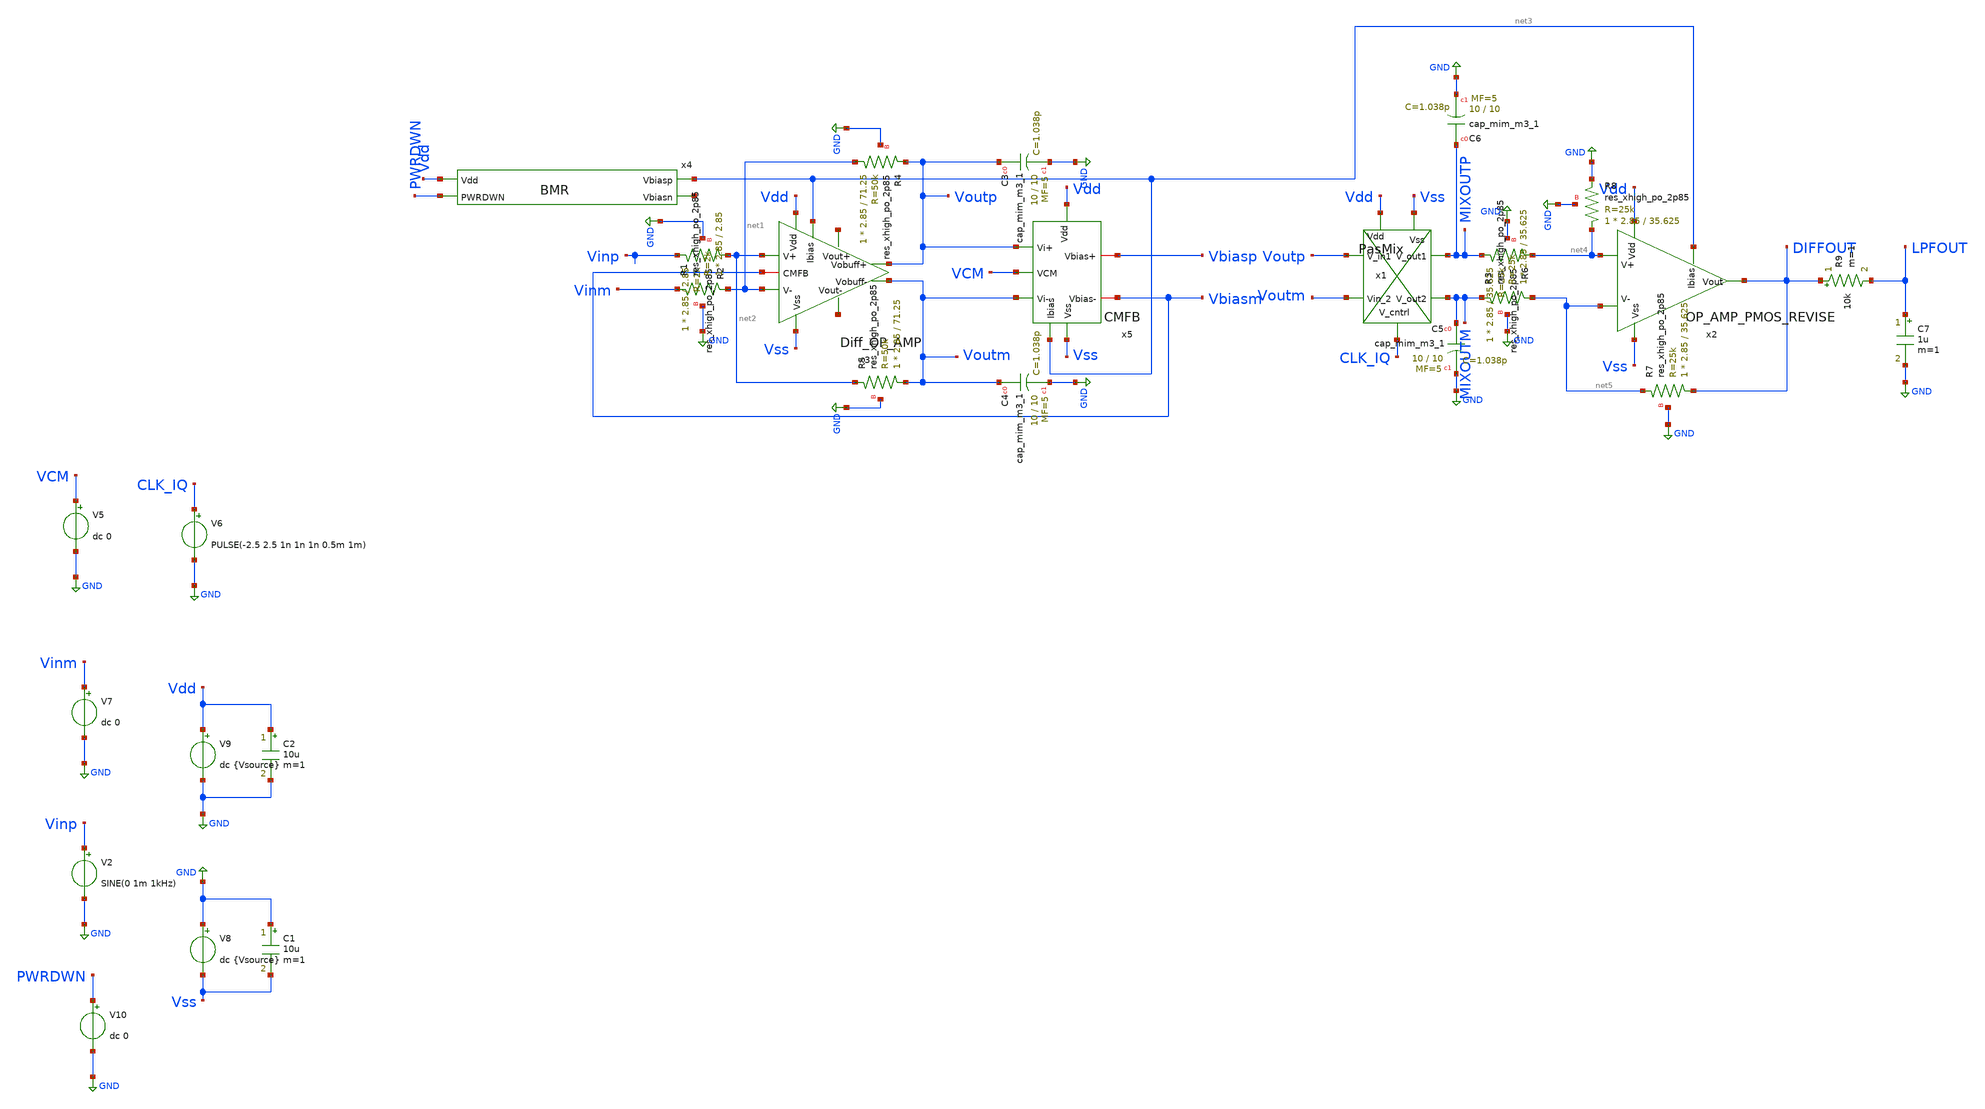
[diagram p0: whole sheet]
** sch_path: xschem/DiffTB.sch
**.subckt DiffTB
V5 VCM GND dc 0
V6 CLK_IQ GND PULSE(-2.5 2.5 1n 1n 1n 0.5m 1m)
V2 Vinp GND SINE(0 1m 1kHz)
V7 Vinm GND dc 0
V8 GND Vss dc {Vsource}
V9 Vdd GND dc {Vsource}
V10 PWRDWN GND dc 0
C1 GND Vss 10u m=1
C2 Vdd GND 10u m=1
x3 Vss Vbiasm net6 net7 net1 net2 Voutp Voutm net3 Vdd Diff_OP_AMP
x4 Vdd net3 net8 PWRDWN BMR
x5 Vss Vbiasp Vbiasm Voutm Voutp VCM net3 Vdd CMFB
XC3 Voutp GND sky130_fd_pr__cap_mim_m3_1 W=10 L=10 MF=5 m=5
XC4 Voutm GND sky130_fd_pr__cap_mim_m3_1 W=10 L=10 MF=5 m=5
XR4 net1 Voutp GND sky130_fd_pr__res_xhigh_po_2p85 L=71.25 mult=1 m=1
XR2 Vinp net2 GND sky130_fd_pr__res_xhigh_po_2p85 L=2.85 mult=1 m=1
XR5 Voutm net2 GND sky130_fd_pr__res_xhigh_po_2p85 L=71.25 mult=1 m=1
XR1 net1 Vinm GND sky130_fd_pr__res_xhigh_po_2p85 L=2.85 mult=1 m=1
x1 Vdd CLK_IQ Vss MIXOUTP Voutp MIXOUTM Voutm PasMix
x2 Vdd Vss net3 DIFFOUT net4 net5 OP_AMP_PMOS_REVISE
XR6 MIXOUTP net4 GND sky130_fd_pr__res_xhigh_po_2p85 L=35.625 mult=1 m=1
XR3 net5 MIXOUTM GND sky130_fd_pr__res_xhigh_po_2p85 L=35.625 mult=1 m=1
XR7 DIFFOUT net5 GND sky130_fd_pr__res_xhigh_po_2p85 L=35.625 mult=1 m=1
XR8 net4 GND GND sky130_fd_pr__res_xhigh_po_2p85 L=35.625 mult=1 m=1
XC5 MIXOUTM GND sky130_fd_pr__cap_mim_m3_1 W=10 L=10 MF=5 m=5
XC6 MIXOUTP GND sky130_fd_pr__cap_mim_m3_1 W=10 L=10 MF=5 m=5
R9 DIFFOUT LPFOUT 10k m=1
C7 LPFOUT GND 1u m=1
**** begin user architecture code


.lib /foss/pdks/sky130A/libs.tech/combined/sky130.lib.spice tt_mm

***Centered at 40C and varies to a range of -20 to 100; with 20C being 1-standard dev***
.param TEMPGAUSS = agauss(40, 60, 3)

***Centered at 2.5V and varies to a range of 2V to 3V; with 0.16mV being 1-standard dev***
.param VOLTGAUSS = agauss(2.5, 0.5, 3)

.param ptemp = 'TEMPGAUSS'

.param Vsource = 'VOLTGAUSS'
.options temp = {ptemp}

.csparam ctemp = {ptemp}
.csparam cvolt = {Vsource}


.control
 let T = 27
 let V = 2.5

 let i_count = 10

 let index = 0

 set wr_vecnames
 dowhile index <= 10
   save all
   tran 10u 50m
   *dc V1 0 6 0.01
   *ac dec 100 0.1 30MEG

   write POST_LPF_OFFSETS_TT_MM_PVT.raw

   set noprintscale

   set appendwrite


   let V = $&cvolt
   let T = $&ctemp

   echo -n This is $&V
   echo -n This is $&T
   echo -n This is $&index

   let index = index + 1
   reset
 end
  **OL AC
  *** print col GAIN_vec UGW_vec PM_vec T_vec V_vec > FDA_AC_CM_GAIN_UGW_PM_SS_PVT.txt
  **Offset
   *** print col OFFSETDIF_vec OFFSETMIX_vec OFFSETOUT_vec T_vec V_vec >
+ PRE_LPF_OFFSETS_SS_MM_PVT.txt

.endc
.end

**** end user architecture code
**.ends

* expanding   symbol:  Diff_OP_AMP.sym # of pins=10
** sym_path: xschem/Diff_OP_AMP.sym
** sch_path: xschem/Diff_OP_AMP.sch
.subckt Diff_OP_AMP Vss CMFB Vout- Vout+ V- V+ Vobuff+ Vobuff- Ibias Vdd
*.opin Vout+
*.ipin Vdd
*.ipin Vss
*.ipin V+
*.ipin V-
*.opin Vout-
*.ipin Ibias
*.opin Vobuff-
*.opin Vobuff+
*.iopin CMFB
XM4 net1 Ibias Vdd Vdd sky130_fd_pr__pfet_g5v0d10v5 L=3 W=31 nf=8 ad='int((8 + 1)/2) * 31 / 8 * 0.29'
+ as='int((8 + 2)/2) * 31 / 8 * 0.29' pd='2*int((8 + 1)/2) * (31 / 8 + 0.29)' ps='2*int((8 + 2)/2) * (31 / 8 + 0.29)'
+ nrd='0.29 / 31 ' nrs='0.29 / 31 ' sa=0 sb=0 sd=0 mult=2 m=2
XM18 net2 V- net1 net1 sky130_fd_pr__pfet_g5v0d10v5 L=3 W=80 nf=8 ad='int((8 + 1)/2) * 80 / 8 * 0.29'
+ as='int((8 + 2)/2) * 80 / 8 * 0.29' pd='2*int((8 + 1)/2) * (80 / 8 + 0.29)' ps='2*int((8 + 2)/2) * (80 / 8 + 0.29)'
+ nrd='0.29 / 80 ' nrs='0.29 / 80 ' sa=0 sb=0 sd=0 mult=4 m=4
XM1 net3 V+ net1 net1 sky130_fd_pr__pfet_g5v0d10v5 L=3 W=80 nf=8 ad='int((8 + 1)/2) * 80 / 8 * 0.29'
+ as='int((8 + 2)/2) * 80 / 8 * 0.29' pd='2*int((8 + 1)/2) * (80 / 8 + 0.29)' ps='2*int((8 + 2)/2) * (80 / 8 + 0.29)'
+ nrd='0.29 / 80 ' nrs='0.29 / 80 ' sa=0 sb=0 sd=0 mult=4 m=4
XM11 net2 CMFB Vss Vss sky130_fd_pr__nfet_g5v0d10v5 L=6 W=0.81 nf=1 ad='int((1 + 1)/2) * 0.81 / 1 * 0.29'
+ as='int((1 + 2)/2) * 0.81 / 1 * 0.29' pd='2*int((1 + 1)/2) * (0.81 / 1 + 0.29)' ps='2*int((1 + 2)/2) * (0.81 / 1 + 0.29)'
+ nrd='0.29 / 0.81 ' nrs='0.29 / 0.81 ' sa=0 sb=0 sd=0 mult=2 m=2
XM3 net3 CMFB Vss Vss sky130_fd_pr__nfet_g5v0d10v5 L=6 W=0.81 nf=1 ad='int((1 + 1)/2) * 0.81 / 1 * 0.29'
+ as='int((1 + 2)/2) * 0.81 / 1 * 0.29' pd='2*int((1 + 1)/2) * (0.81 / 1 + 0.29)' ps='2*int((1 + 2)/2) * (0.81 / 1 + 0.29)'
+ nrd='0.29 / 0.81 ' nrs='0.29 / 0.81 ' sa=0 sb=0 sd=0 mult=2 m=2
XM13 Vout+ net2 Vss Vss sky130_fd_pr__nfet_g5v0d10v5 L=3 W=14 nf=2 ad='int((2 + 1)/2) * 14 / 2 * 0.29'
+ as='int((2 + 2)/2) * 14 / 2 * 0.29' pd='2*int((2 + 1)/2) * (14 / 2 + 0.29)' ps='2*int((2 + 2)/2) * (14 / 2 + 0.29)'
+ nrd='0.29 / 14 ' nrs='0.29 / 14 ' sa=0 sb=0 sd=0 mult=2 m=2
XM2 Vout- net3 Vss Vss sky130_fd_pr__nfet_g5v0d10v5 L=3 W=14 nf=2 ad='int((2 + 1)/2) * 14 / 2 * 0.29'
+ as='int((2 + 2)/2) * 14 / 2 * 0.29' pd='2*int((2 + 1)/2) * (14 / 2 + 0.29)' ps='2*int((2 + 2)/2) * (14 / 2 + 0.29)'
+ nrd='0.29 / 14 ' nrs='0.29 / 14 ' sa=0 sb=0 sd=0 mult=2 m=2
XM5 net5 Ibias Vdd Vdd sky130_fd_pr__pfet_g5v0d10v5 L=3 W=31 nf=8 ad='int((8 + 1)/2) * 31 / 8 * 0.29'
+ as='int((8 + 2)/2) * 31 / 8 * 0.29' pd='2*int((8 + 1)/2) * (31 / 8 + 0.29)' ps='2*int((8 + 2)/2) * (31 / 8 + 0.29)'
+ nrd='0.29 / 31 ' nrs='0.29 / 31 ' sa=0 sb=0 sd=0 mult=30 m=30
XM6 net7 Ibias Vdd Vdd sky130_fd_pr__pfet_g5v0d10v5 L=3 W=31 nf=8 ad='int((8 + 1)/2) * 31 / 8 * 0.29'
+ as='int((8 + 2)/2) * 31 / 8 * 0.29' pd='2*int((8 + 1)/2) * (31 / 8 + 0.29)' ps='2*int((8 + 2)/2) * (31 / 8 + 0.29)'
+ nrd='0.29 / 31 ' nrs='0.29 / 31 ' sa=0 sb=0 sd=0 mult=30 m=30
XM8 Vout+ Vout+ net4 net4 sky130_fd_pr__pfet_g5v0d10v5 L=3 W=41.1 nf=4 ad='int((4 + 1)/2) * 41.1 / 4 * 0.29'
+ as='int((4 + 2)/2) * 41.1 / 4 * 0.29' pd='2*int((4 + 1)/2) * (41.1 / 4 + 0.29)' ps='2*int((4 + 2)/2) * (41.1 / 4 + 0.29)'
+ nrd='0.29 / 41.1 ' nrs='0.29 / 41.1 ' sa=0 sb=0 sd=0 mult=4 m=4
XM7 Vss Vout+ Vobuff- Vobuff- sky130_fd_pr__pfet_g5v0d10v5 L=3 W=41.1 nf=4 ad='int((4 + 1)/2) * 41.1 / 4 * 0.29'
+ as='int((4 + 2)/2) * 41.1 / 4 * 0.29' pd='2*int((4 + 1)/2) * (41.1 / 4 + 0.29)' ps='2*int((4 + 2)/2) * (41.1 / 4 + 0.29)'
+ nrd='0.29 / 41.1 ' nrs='0.29 / 41.1 ' sa=0 sb=0 sd=0 mult=4 m=4
XM9 Vss Vout- Vobuff+ Vobuff+ sky130_fd_pr__pfet_g5v0d10v5 L=3 W=41.1 nf=4 ad='int((4 + 1)/2) * 41.1 / 4 * 0.29'
+ as='int((4 + 2)/2) * 41.1 / 4 * 0.29' pd='2*int((4 + 1)/2) * (41.1 / 4 + 0.29)' ps='2*int((4 + 2)/2) * (41.1 / 4 + 0.29)'
+ nrd='0.29 / 41.1 ' nrs='0.29 / 41.1 ' sa=0 sb=0 sd=0 mult=4 m=4
XM12 Vout- Vout- net6 net6 sky130_fd_pr__pfet_g5v0d10v5 L=3 W=41.1 nf=4 ad='int((4 + 1)/2) * 41.1 / 4 * 0.29'
+ as='int((4 + 2)/2) * 41.1 / 4 * 0.29' pd='2*int((4 + 1)/2) * (41.1 / 4 + 0.29)' ps='2*int((4 + 2)/2) * (41.1 / 4 + 0.29)'
+ nrd='0.29 / 41.1 ' nrs='0.29 / 41.1 ' sa=0 sb=0 sd=0 mult=4 m=4
XM16 net5 net5 net4 net4 sky130_fd_pr__nfet_g5v0d10v5 L=3 W=18 nf=4 ad='int((4 + 1)/2) * 18 / 4 * 0.29'
+ as='int((4 + 2)/2) * 18 / 4 * 0.29' pd='2*int((4 + 1)/2) * (18 / 4 + 0.29)' ps='2*int((4 + 2)/2) * (18 / 4 + 0.29)'
+ nrd='0.29 / 18 ' nrs='0.29 / 18 ' sa=0 sb=0 sd=0 mult=2 m=2
XM14 Vdd net5 Vobuff- Vobuff- sky130_fd_pr__nfet_g5v0d10v5 L=3 W=18 nf=4 ad='int((4 + 1)/2) * 18 / 4 * 0.29'
+ as='int((4 + 2)/2) * 18 / 4 * 0.29' pd='2*int((4 + 1)/2) * (18 / 4 + 0.29)' ps='2*int((4 + 2)/2) * (18 / 4 + 0.29)'
+ nrd='0.29 / 18 ' nrs='0.29 / 18 ' sa=0 sb=0 sd=0 mult=2 m=2
XM10 Vdd net7 Vobuff+ Vobuff+ sky130_fd_pr__nfet_g5v0d10v5 L=3 W=18 nf=4 ad='int((4 + 1)/2) * 18 / 4 * 0.29'
+ as='int((4 + 2)/2) * 18 / 4 * 0.29' pd='2*int((4 + 1)/2) * (18 / 4 + 0.29)' ps='2*int((4 + 2)/2) * (18 / 4 + 0.29)'
+ nrd='0.29 / 18 ' nrs='0.29 / 18 ' sa=0 sb=0 sd=0 mult=2 m=2
XM15 net7 net7 net6 net6 sky130_fd_pr__nfet_g5v0d10v5 L=3 W=18 nf=4 ad='int((4 + 1)/2) * 18 / 4 * 0.29'
+ as='int((4 + 2)/2) * 18 / 4 * 0.29' pd='2*int((4 + 1)/2) * (18 / 4 + 0.29)' ps='2*int((4 + 2)/2) * (18 / 4 + 0.29)'
+ nrd='0.29 / 18 ' nrs='0.29 / 18 ' sa=0 sb=0 sd=0 mult=2 m=2
XC10 net2 Vout+ sky130_fd_pr__cap_mim_m3_1 W=10 L=10 MF=5 m=5
XC1 net3 Vout- sky130_fd_pr__cap_mim_m3_1 W=10 L=10 MF=5 m=5
.ends


* expanding   symbol:  BMR.sym # of pins=4
** sym_path: xschem/BMR.sym
** sch_path: xschem/BMR.sch
.subckt BMR Vdd Vbiasp Vbiasn PWRDWN
*.ipin Vdd
*.opin Vbiasn
*.opin Vbiasp
*.ipin PWRDWN
XM3 Vbiasn Vbiasn GND GND sky130_fd_pr__nfet_g5v0d10v5 L=3 W=1.4 nf=1 ad='int((1 + 1)/2) * 1.4 / 1 * 0.29'
+ as='int((1 + 2)/2) * 1.4 / 1 * 0.29' pd='2*int((1 + 1)/2) * (1.4 / 1 + 0.29)' ps='2*int((1 + 2)/2) * (1.4 / 1 + 0.29)'
+ nrd='0.29 / 1.4 ' nrs='0.29 / 1.4 ' sa=0 sb=0 sd=0 mult=1 m=1
XM1 Vbiasp Vbiasp Vdd Vdd sky130_fd_pr__pfet_g5v0d10v5 L=3 W=31 nf=8 ad='int((8 + 1)/2) * 31 / 8 * 0.29'
+ as='int((8 + 2)/2) * 31 / 8 * 0.29' pd='2*int((8 + 1)/2) * (31 / 8 + 0.29)' ps='2*int((8 + 2)/2) * (31 / 8 + 0.29)'
+ nrd='0.29 / 31 ' nrs='0.29 / 31 ' sa=0 sb=0 sd=0 mult=2 m=2
XM2 Vbiasn Vbiasp Vdd Vdd sky130_fd_pr__pfet_g5v0d10v5 L=3 W=31 nf=8 ad='int((8 + 1)/2) * 31 / 8 * 0.29'
+ as='int((8 + 2)/2) * 31 / 8 * 0.29' pd='2*int((8 + 1)/2) * (31 / 8 + 0.29)' ps='2*int((8 + 2)/2) * (31 / 8 + 0.29)'
+ nrd='0.29 / 31 ' nrs='0.29 / 31 ' sa=0 sb=0 sd=0 mult=2 m=2
XM11 net1 PWRUP Vdd Vdd sky130_fd_pr__pfet_g5v0d10v5 L=10 W=1 nf=1 ad='int((1 + 1)/2) * 1 / 1 * 0.29'
+ as='int((1 + 2)/2) * 1 / 1 * 0.29' pd='2*int((1 + 1)/2) * (1 / 1 + 0.29)' ps='2*int((1 + 2)/2) * (1 / 1 + 0.29)'
+ nrd='0.29 / 1 ' nrs='0.29 / 1 ' sa=0 sb=0 sd=0 mult=1 m=1
XM4 Vbiasp Vbiasn net2 GND sky130_fd_pr__nfet_g5v0d10v5 L=3 W=1.4 nf=1 ad='int((1 + 1)/2) * 1.4 / 1 * 0.29'
+ as='int((1 + 2)/2) * 1.4 / 1 * 0.29' pd='2*int((1 + 1)/2) * (1.4 / 1 + 0.29)' ps='2*int((1 + 2)/2) * (1.4 / 1 + 0.29)'
+ nrd='0.29 / 1.4 ' nrs='0.29 / 1.4 ' sa=0 sb=0 sd=0 mult=2 m=2
XM5 net1 Vbiasn GND GND sky130_fd_pr__nfet_g5v0d10v5 L=3 W=1.4 nf=1 ad='int((1 + 1)/2) * 1.4 / 1 * 0.29'
+ as='int((1 + 2)/2) * 1.4 / 1 * 0.29' pd='2*int((1 + 1)/2) * (1.4 / 1 + 0.29)' ps='2*int((1 + 2)/2) * (1.4 / 1 + 0.29)'
+ nrd='0.29 / 1.4 ' nrs='0.29 / 1.4 ' sa=0 sb=0 sd=0 mult=1 m=1
XM7 net3 net1 Vbiasn GND sky130_fd_pr__nfet_g5v0d10v5 L=1 W=20 nf=1 ad='int((1 + 1)/2) * 20 / 1 * 0.29'
+ as='int((1 + 2)/2) * 20 / 1 * 0.29' pd='2*int((1 + 1)/2) * (20 / 1 + 0.29)' ps='2*int((1 + 2)/2) * (20 / 1 + 0.29)'
+ nrd='0.29 / 20 ' nrs='0.29 / 20 ' sa=0 sb=0 sd=0 mult=1 m=1
x1 Vdd PWRUP PWRDWN GND NOT_GATE
XM12 Vbiasp PWRUP net3 GND sky130_fd_pr__nfet_g5v0d10v5 L=1 W=20 nf=1 ad='int((1 + 1)/2) * 20 / 1 * 0.29'
+ as='int((1 + 2)/2) * 20 / 1 * 0.29' pd='2*int((1 + 1)/2) * (20 / 1 + 0.29)' ps='2*int((1 + 2)/2) * (20 / 1 + 0.29)'
+ nrd='0.29 / 20 ' nrs='0.29 / 20 ' sa=0 sb=0 sd=0 mult=1 m=1
XM9 Vbiasp PWRUP Vdd Vdd sky130_fd_pr__pfet_g5v0d10v5 L=1 W=3 nf=1 ad='int((1 + 1)/2) * 3 / 1 * 0.29'
+ as='int((1 + 2)/2) * 3 / 1 * 0.29' pd='2*int((1 + 1)/2) * (3 / 1 + 0.29)' ps='2*int((1 + 2)/2) * (3 / 1 + 0.29)'
+ nrd='0.29 / 3 ' nrs='0.29 / 3 ' sa=0 sb=0 sd=0 mult=1 m=1
XM10 Vbiasn PWRDWN GND GND sky130_fd_pr__nfet_g5v0d10v5 L=1 W=1 nf=1 ad='int((1 + 1)/2) * 1 / 1 * 0.29'
+ as='int((1 + 2)/2) * 1 / 1 * 0.29' pd='2*int((1 + 1)/2) * (1 / 1 + 0.29)' ps='2*int((1 + 2)/2) * (1 / 1 + 0.29)'
+ nrd='0.29 / 1 ' nrs='0.29 / 1 ' sa=0 sb=0 sd=0 mult=1 m=1
XR5 GND net2 GND sky130_fd_pr__res_xhigh_po_2p85 L=71.25 mult=1 m=1
XC10 Vdd net1 sky130_fd_pr__cap_mim_m3_1 W=10 L=10 MF=5 m=5
XC2 Vdd Vbiasp sky130_fd_pr__cap_mim_m3_1 W=10 L=10 MF=5 m=5
XC1 Vbiasn GND sky130_fd_pr__cap_mim_m3_1 W=10 L=10 MF=5 m=5
.ends


* expanding   symbol:  CMFB.sym # of pins=8
** sym_path: xschem/CMFB.sym
** sch_path: xschem/CMFB.sch
.subckt CMFB Vss Vbias+ Vbias- Vi- Vi+ VCM Ibias Vdd
*.ipin VCM
*.ipin Vss
*.ipin Vdd
*.ipin Vi+
*.ipin Vi-
*.ipin Ibias
*.iopin Vbias+
*.iopin Vbias-
XM9 net1 Ibias Vdd Vdd sky130_fd_pr__pfet_g5v0d10v5 L=3 W=31 nf=8 ad='int((8 + 1)/2) * 31 / 8 * 0.29'
+ as='int((8 + 2)/2) * 31 / 8 * 0.29' pd='2*int((8 + 1)/2) * (31 / 8 + 0.29)' ps='2*int((8 + 2)/2) * (31 / 8 + 0.29)'
+ nrd='0.29 / 31 ' nrs='0.29 / 31 ' sa=0 sb=0 sd=0 mult=1 m=1
XM1 net2 Ibias Vdd Vdd sky130_fd_pr__pfet_g5v0d10v5 L=3 W=31 nf=8 ad='int((8 + 1)/2) * 31 / 8 * 0.29'
+ as='int((8 + 2)/2) * 31 / 8 * 0.29' pd='2*int((8 + 1)/2) * (31 / 8 + 0.29)' ps='2*int((8 + 2)/2) * (31 / 8 + 0.29)'
+ nrd='0.29 / 31 ' nrs='0.29 / 31 ' sa=0 sb=0 sd=0 mult=1 m=1
XM5 Vbias- Vi+ net1 net1 sky130_fd_pr__pfet_g5v0d10v5 L=1 W=28 nf=4 ad='int((4 + 1)/2) * 28 / 4 * 0.29'
+ as='int((4 + 2)/2) * 28 / 4 * 0.29' pd='2*int((4 + 1)/2) * (28 / 4 + 0.29)' ps='2*int((4 + 2)/2) * (28 / 4 + 0.29)'
+ nrd='0.29 / 28 ' nrs='0.29 / 28 ' sa=0 sb=0 sd=0 mult=2 m=2
XM2 Vbias+ VCM net2 net2 sky130_fd_pr__pfet_g5v0d10v5 L=1 W=28 nf=4 ad='int((4 + 1)/2) * 28 / 4 * 0.29'
+ as='int((4 + 2)/2) * 28 / 4 * 0.29' pd='2*int((4 + 1)/2) * (28 / 4 + 0.29)' ps='2*int((4 + 2)/2) * (28 / 4 + 0.29)'
+ nrd='0.29 / 28 ' nrs='0.29 / 28 ' sa=0 sb=0 sd=0 mult=2 m=2
XM4 Vbias+ VCM net1 net1 sky130_fd_pr__pfet_g5v0d10v5 L=1 W=28 nf=4 ad='int((4 + 1)/2) * 28 / 4 * 0.29'
+ as='int((4 + 2)/2) * 28 / 4 * 0.29' pd='2*int((4 + 1)/2) * (28 / 4 + 0.29)' ps='2*int((4 + 2)/2) * (28 / 4 + 0.29)'
+ nrd='0.29 / 28 ' nrs='0.29 / 28 ' sa=0 sb=0 sd=0 mult=2 m=2
XM3 Vbias- Vi- net2 net2 sky130_fd_pr__pfet_g5v0d10v5 L=1 W=28 nf=4 ad='int((4 + 1)/2) * 28 / 4 * 0.29'
+ as='int((4 + 2)/2) * 28 / 4 * 0.29' pd='2*int((4 + 1)/2) * (28 / 4 + 0.29)' ps='2*int((4 + 2)/2) * (28 / 4 + 0.29)'
+ nrd='0.29 / 28 ' nrs='0.29 / 28 ' sa=0 sb=0 sd=0 mult=2 m=2
XM6 Vbias+ Vbias+ Vss Vss sky130_fd_pr__nfet_g5v0d10v5 L=6 W=0.81 nf=1 ad='int((1 + 1)/2) * 0.81 / 1 * 0.29'
+ as='int((1 + 2)/2) * 0.81 / 1 * 0.29' pd='2*int((1 + 1)/2) * (0.81 / 1 + 0.29)' ps='2*int((1 + 2)/2) * (0.81 / 1 + 0.29)'
+ nrd='0.29 / 0.81 ' nrs='0.29 / 0.81 ' sa=0 sb=0 sd=0 mult=2 m=2
XM7 Vbias- Vbias- Vss Vss sky130_fd_pr__nfet_g5v0d10v5 L=6 W=0.81 nf=1 ad='int((1 + 1)/2) * 0.81 / 1 * 0.29'
+ as='int((1 + 2)/2) * 0.81 / 1 * 0.29' pd='2*int((1 + 1)/2) * (0.81 / 1 + 0.29)' ps='2*int((1 + 2)/2) * (0.81 / 1 + 0.29)'
+ nrd='0.29 / 0.81 ' nrs='0.29 / 0.81 ' sa=0 sb=0 sd=0 mult=2 m=2
.ends


* expanding   symbol:  PasMix.sym # of pins=7
** sym_path: xschem/PasMix.sym
** sch_path: xschem/PasMix.sch
.subckt PasMix Vdd V_cntrl Vss V_out1 V_in1 V_out2 Vin_2
*.ipin V_in1
*.ipin Vin_2
*.opin V_out1
*.opin V_out2
*.ipin Vdd
*.ipin Vss
*.ipin V_cntrl
x1 V_Invert V_in1 V_out1 Vdd Vss V_CLK T-gate
x2 V_Invert Vin_2 V_out2 Vdd Vss V_CLK T-gate
x3 V_CLK Vin_2 V_out1 Vdd Vss V_Invert T-gate
x4 V_CLK V_in1 V_out2 Vdd Vss V_Invert T-gate
XM3 net1 V_cntrl Vss Vss sky130_fd_pr__nfet_g5v0d10v5 L=1 W=1 nf=1 ad='int((1 + 1)/2) * 1 / 1 * 0.29'
+ as='int((1 + 2)/2) * 1 / 1 * 0.29' pd='2*int((1 + 1)/2) * (1 / 1 + 0.29)' ps='2*int((1 + 2)/2) * (1 / 1 + 0.29)'
+ nrd='0.29 / 1 ' nrs='0.29 / 1 ' sa=0 sb=0 sd=0 mult=1 m=1
XM4 net1 V_cntrl Vdd Vdd sky130_fd_pr__pfet_g5v0d10v5 L=1 W=3 nf=1 ad='int((1 + 1)/2) * 3 / 1 * 0.29'
+ as='int((1 + 2)/2) * 3 / 1 * 0.29' pd='2*int((1 + 1)/2) * (3 / 1 + 0.29)' ps='2*int((1 + 2)/2) * (3 / 1 + 0.29)'
+ nrd='0.29 / 3 ' nrs='0.29 / 3 ' sa=0 sb=0 sd=0 mult=1 m=1
XM5 V_CLK net1 Vss Vss sky130_fd_pr__nfet_g5v0d10v5 L=1 W=3 nf=1 ad='int((1 + 1)/2) * 3 / 1 * 0.29' as='int((1 + 2)/2) * 3 / 1 * 0.29'
+ pd='2*int((1 + 1)/2) * (3 / 1 + 0.29)' ps='2*int((1 + 2)/2) * (3 / 1 + 0.29)' nrd='0.29 / 3 ' nrs='0.29 / 3 '
+ sa=0 sb=0 sd=0 mult=1 m=1
XM6 V_CLK net1 Vdd Vdd sky130_fd_pr__pfet_g5v0d10v5 L=1 W=27 nf=1 ad='int((1 + 1)/2) * 27 / 1 * 0.29'
+ as='int((1 + 2)/2) * 27 / 1 * 0.29' pd='2*int((1 + 1)/2) * (27 / 1 + 0.29)' ps='2*int((1 + 2)/2) * (27 / 1 + 0.29)'
+ nrd='0.29 / 27 ' nrs='0.29 / 27 ' sa=0 sb=0 sd=0 mult=1 m=1
XM7 net2 net1 Vss Vss sky130_fd_pr__nfet_g5v0d10v5 L=1 W=3 nf=1 ad='int((1 + 1)/2) * 3 / 1 * 0.29' as='int((1 + 2)/2) * 3 / 1 * 0.29'
+ pd='2*int((1 + 1)/2) * (3 / 1 + 0.29)' ps='2*int((1 + 2)/2) * (3 / 1 + 0.29)' nrd='0.29 / 3 ' nrs='0.29 / 3 '
+ sa=0 sb=0 sd=0 mult=1 m=1
XM8 net2 net1 Vdd Vdd sky130_fd_pr__pfet_g5v0d10v5 L=1 W=27 nf=1 ad='int((1 + 1)/2) * 27 / 1 * 0.29'
+ as='int((1 + 2)/2) * 27 / 1 * 0.29' pd='2*int((1 + 1)/2) * (27 / 1 + 0.29)' ps='2*int((1 + 2)/2) * (27 / 1 + 0.29)'
+ nrd='0.29 / 27 ' nrs='0.29 / 27 ' sa=0 sb=0 sd=0 mult=1 m=1
XM9 V_Invert net2 Vss Vss sky130_fd_pr__nfet_g5v0d10v5 L=1 W=3 nf=1 ad='int((1 + 1)/2) * 3 / 1 * 0.29'
+ as='int((1 + 2)/2) * 3 / 1 * 0.29' pd='2*int((1 + 1)/2) * (3 / 1 + 0.29)' ps='2*int((1 + 2)/2) * (3 / 1 + 0.29)'
+ nrd='0.29 / 3 ' nrs='0.29 / 3 ' sa=0 sb=0 sd=0 mult=1 m=1
XM10 V_Invert net2 Vdd Vdd sky130_fd_pr__pfet_g5v0d10v5 L=1 W=27 nf=1 ad='int((1 + 1)/2) * 27 / 1 * 0.29'
+ as='int((1 + 2)/2) * 27 / 1 * 0.29' pd='2*int((1 + 1)/2) * (27 / 1 + 0.29)' ps='2*int((1 + 2)/2) * (27 / 1 + 0.29)'
+ nrd='0.29 / 27 ' nrs='0.29 / 27 ' sa=0 sb=0 sd=0 mult=1 m=1
.ends


* expanding   symbol:  OP_AMP_PMOS_REVISE.sym # of pins=6
** sym_path: xschem/OP_AMP_PMOS_REVISE.sym
** sch_path: xschem/OP_AMP_PMOS_REVISE.sch
.subckt OP_AMP_PMOS_REVISE Vdd Vss Ibias Vout V+ V-
*.ipin V-
*.ipin V+
*.ipin Vdd
*.ipin Vss
*.ipin Ibias
*.opin Vout
XM3 net2 net1 Vss Vss sky130_fd_pr__nfet_g5v0d10v5 L=6 W=0.81 nf=1 ad='int((1 + 1)/2) * 0.81 / 1 * 0.29'
+ as='int((1 + 2)/2) * 0.81 / 1 * 0.29' pd='2*int((1 + 1)/2) * (0.81 / 1 + 0.29)' ps='2*int((1 + 2)/2) * (0.81 / 1 + 0.29)'
+ nrd='0.29 / 0.81 ' nrs='0.29 / 0.81 ' sa=0 sb=0 sd=0 mult=2 m=2
XM1 net2 V+ net3 net3 sky130_fd_pr__pfet_g5v0d10v5 L=3 W=80 nf=8 ad='int((8 + 1)/2) * 80 / 8 * 0.29'
+ as='int((8 + 2)/2) * 80 / 8 * 0.29' pd='2*int((8 + 1)/2) * (80 / 8 + 0.29)' ps='2*int((8 + 2)/2) * (80 / 8 + 0.29)'
+ nrd='0.29 / 80 ' nrs='0.29 / 80 ' sa=0 sb=0 sd=0 mult=4 m=4
XM2 net1 V- net3 net3 sky130_fd_pr__pfet_g5v0d10v5 L=3 W=80 nf=8 ad='int((8 + 1)/2) * 80 / 8 * 0.29'
+ as='int((8 + 2)/2) * 80 / 8 * 0.29' pd='2*int((8 + 1)/2) * (80 / 8 + 0.29)' ps='2*int((8 + 2)/2) * (80 / 8 + 0.29)'
+ nrd='0.29 / 80 ' nrs='0.29 / 80 ' sa=0 sb=0 sd=0 mult=4 m=4
XM4 net1 net1 Vss Vss sky130_fd_pr__nfet_g5v0d10v5 L=6 W=0.81 nf=1 ad='int((1 + 1)/2) * 0.81 / 1 * 0.29'
+ as='int((1 + 2)/2) * 0.81 / 1 * 0.29' pd='2*int((1 + 1)/2) * (0.81 / 1 + 0.29)' ps='2*int((1 + 2)/2) * (0.81 / 1 + 0.29)'
+ nrd='0.29 / 0.81 ' nrs='0.29 / 0.81 ' sa=0 sb=0 sd=0 mult=2 m=2
XM8 net4 net2 Vss Vss sky130_fd_pr__nfet_g5v0d10v5 L=3 W=14 nf=4 ad='int((4 + 1)/2) * 14 / 4 * 0.29'
+ as='int((4 + 2)/2) * 14 / 4 * 0.29' pd='2*int((4 + 1)/2) * (14 / 4 + 0.29)' ps='2*int((4 + 2)/2) * (14 / 4 + 0.29)'
+ nrd='0.29 / 14 ' nrs='0.29 / 14 ' sa=0 sb=0 sd=0 mult=2 m=2
XM5 net3 Ibias Vdd Vdd sky130_fd_pr__pfet_g5v0d10v5 L=3 W=31 nf=8 ad='int((8 + 1)/2) * 31 / 8 * 0.29'
+ as='int((8 + 2)/2) * 31 / 8 * 0.29' pd='2*int((8 + 1)/2) * (31 / 8 + 0.29)' ps='2*int((8 + 2)/2) * (31 / 8 + 0.29)'
+ nrd='0.29 / 31 ' nrs='0.29 / 31 ' sa=0 sb=0 sd=0 mult=2 m=2
XM6 net6 Ibias Vdd Vdd sky130_fd_pr__pfet_g5v0d10v5 L=3 W=31 nf=8 ad='int((8 + 1)/2) * 31 / 8 * 0.29'
+ as='int((8 + 2)/2) * 31 / 8 * 0.29' pd='2*int((8 + 1)/2) * (31 / 8 + 0.29)' ps='2*int((8 + 2)/2) * (31 / 8 + 0.29)'
+ nrd='0.29 / 31 ' nrs='0.29 / 31 ' sa=0 sb=0 sd=0 mult=30 m=30
XM7 net4 net4 net5 net5 sky130_fd_pr__pfet_g5v0d10v5 L=3 W=41.1 nf=4 ad='int((4 + 1)/2) * 41.1 / 4 * 0.29'
+ as='int((4 + 2)/2) * 41.1 / 4 * 0.29' pd='2*int((4 + 1)/2) * (41.1 / 4 + 0.29)' ps='2*int((4 + 2)/2) * (41.1 / 4 + 0.29)'
+ nrd='0.29 / 41.1 ' nrs='0.29 / 41.1 ' sa=0 sb=0 sd=0 mult=4 m=4
XM9 Vss net4 Vout Vout sky130_fd_pr__pfet_g5v0d10v5 L=3 W=41.1 nf=4 ad='int((4 + 1)/2) * 41.1 / 4 * 0.29'
+ as='int((4 + 2)/2) * 41.1 / 4 * 0.29' pd='2*int((4 + 1)/2) * (41.1 / 4 + 0.29)' ps='2*int((4 + 2)/2) * (41.1 / 4 + 0.29)'
+ nrd='0.29 / 41.1 ' nrs='0.29 / 41.1 ' sa=0 sb=0 sd=0 mult=4 m=4
XM10 net6 net6 net5 net5 sky130_fd_pr__nfet_g5v0d10v5 L=3 W=18 nf=4 ad='int((4 + 1)/2) * 18 / 4 * 0.29'
+ as='int((4 + 2)/2) * 18 / 4 * 0.29' pd='2*int((4 + 1)/2) * (18 / 4 + 0.29)' ps='2*int((4 + 2)/2) * (18 / 4 + 0.29)'
+ nrd='0.29 / 18 ' nrs='0.29 / 18 ' sa=0 sb=0 sd=0 mult=2 m=2
XM11 Vdd net6 Vout Vout sky130_fd_pr__nfet_g5v0d10v5 L=3 W=18 nf=4 ad='int((4 + 1)/2) * 18 / 4 * 0.29'
+ as='int((4 + 2)/2) * 18 / 4 * 0.29' pd='2*int((4 + 1)/2) * (18 / 4 + 0.29)' ps='2*int((4 + 2)/2) * (18 / 4 + 0.29)'
+ nrd='0.29 / 18 ' nrs='0.29 / 18 ' sa=0 sb=0 sd=0 mult=2 m=2
XC10 net2 net4 sky130_fd_pr__cap_mim_m3_1 W=10 L=10 MF=5 m=5
.ends


* expanding   symbol:  NOT_GATE.sym # of pins=4
** sym_path: xschem/NOT_GATE.sym
** sch_path: xschem/NOT_GATE.sch
.subckt NOT_GATE Vdd Vout Vin Vss
*.opin Vout
*.ipin Vdd
*.ipin Vss
*.ipin Vin
XM1 Vout Vin Vss Vss sky130_fd_pr__nfet_g5v0d10v5 L=1 W=1 nf=1 ad='int((1 + 1)/2) * 1 / 1 * 0.29' as='int((1 + 2)/2) * 1 / 1 * 0.29'
+ pd='2*int((1 + 1)/2) * (1 / 1 + 0.29)' ps='2*int((1 + 2)/2) * (1 / 1 + 0.29)' nrd='0.29 / 1 ' nrs='0.29 / 1 '
+ sa=0 sb=0 sd=0 mult=1 m=1
XM2 Vout Vin Vdd Vdd sky130_fd_pr__pfet_g5v0d10v5 L=1 W=3 nf=1 ad='int((1 + 1)/2) * 3 / 1 * 0.29' as='int((1 + 2)/2) * 3 / 1 * 0.29'
+ pd='2*int((1 + 1)/2) * (3 / 1 + 0.29)' ps='2*int((1 + 2)/2) * (3 / 1 + 0.29)' nrd='0.29 / 3 ' nrs='0.29 / 3 '
+ sa=0 sb=0 sd=0 mult=1 m=1
.ends


* expanding   symbol:  T-gate.sym # of pins=6
** sym_path: xschem/T-gate.sym
** sch_path: xschem/T-gate.sch
.subckt T-gate I_CLK T_In T_Out Vdd Vss CLK
*.ipin T_In
*.opin T_Out
*.ipin Vdd
*.ipin Vss
*.ipin I_CLK
*.ipin CLK
XM1 T_In I_CLK T_Out Vdd sky130_fd_pr__pfet_g5v0d10v5 L=0.5 W=3 nf=1 ad='int((1 + 1)/2) * 3 / 1 * 0.29'
+ as='int((1 + 2)/2) * 3 / 1 * 0.29' pd='2*int((1 + 1)/2) * (3 / 1 + 0.29)' ps='2*int((1 + 2)/2) * (3 / 1 + 0.29)'
+ nrd='0.29 / 3 ' nrs='0.29 / 3 ' sa=0 sb=0 sd=0 mult=1 m=1
XM3 T_Out CLK T_In Vss sky130_fd_pr__nfet_g5v0d10v5 L=0.5 W=1 nf=1 ad='int((1 + 1)/2) * 1 / 1 * 0.29'
+ as='int((1 + 2)/2) * 1 / 1 * 0.29' pd='2*int((1 + 1)/2) * (1 / 1 + 0.29)' ps='2*int((1 + 2)/2) * (1 / 1 + 0.29)'
+ nrd='0.29 / 1 ' nrs='0.29 / 1 ' sa=0 sb=0 sd=0 mult=1 m=1
XM2 T_Out CLK T_Out Vdd sky130_fd_pr__pfet_g5v0d10v5 L=0.5 W=1.5 nf=1 ad='int((1 + 1)/2) * 1.5 / 1 * 0.29'
+ as='int((1 + 2)/2) * 1.5 / 1 * 0.29' pd='2*int((1 + 1)/2) * (1.5 / 1 + 0.29)' ps='2*int((1 + 2)/2) * (1.5 / 1 + 0.29)'
+ nrd='0.29 / 1.5 ' nrs='0.29 / 1.5 ' sa=0 sb=0 sd=0 mult=1 m=1
XM4 T_In CLK T_In Vdd sky130_fd_pr__pfet_g5v0d10v5 L=0.5 W=1.5 nf=1 ad='int((1 + 1)/2) * 1.5 / 1 * 0.29'
+ as='int((1 + 2)/2) * 1.5 / 1 * 0.29' pd='2*int((1 + 1)/2) * (1.5 / 1 + 0.29)' ps='2*int((1 + 2)/2) * (1.5 / 1 + 0.29)'
+ nrd='0.29 / 1.5 ' nrs='0.29 / 1.5 ' sa=0 sb=0 sd=0 mult=1 m=1
XM5 T_In I_CLK T_In Vss sky130_fd_pr__nfet_g5v0d10v5 L=0.5 W=0.5 nf=1 ad='int((1 + 1)/2) * 0.5 / 1 * 0.29'
+ as='int((1 + 2)/2) * 0.5 / 1 * 0.29' pd='2*int((1 + 1)/2) * (0.5 / 1 + 0.29)' ps='2*int((1 + 2)/2) * (0.5 / 1 + 0.29)'
+ nrd='0.29 / 0.5 ' nrs='0.29 / 0.5 ' sa=0 sb=0 sd=0 mult=1 m=1
XM6 T_Out I_CLK T_Out Vss sky130_fd_pr__nfet_g5v0d10v5 L=0.5 W=0.5 nf=1 ad='int((1 + 1)/2) * 0.5 / 1 * 0.29'
+ as='int((1 + 2)/2) * 0.5 / 1 * 0.29' pd='2*int((1 + 1)/2) * (0.5 / 1 + 0.29)' ps='2*int((1 + 2)/2) * (0.5 / 1 + 0.29)'
+ nrd='0.29 / 0.5 ' nrs='0.29 / 0.5 ' sa=0 sb=0 sd=0 mult=1 m=1
.ends

.GLOBAL GND
.end
